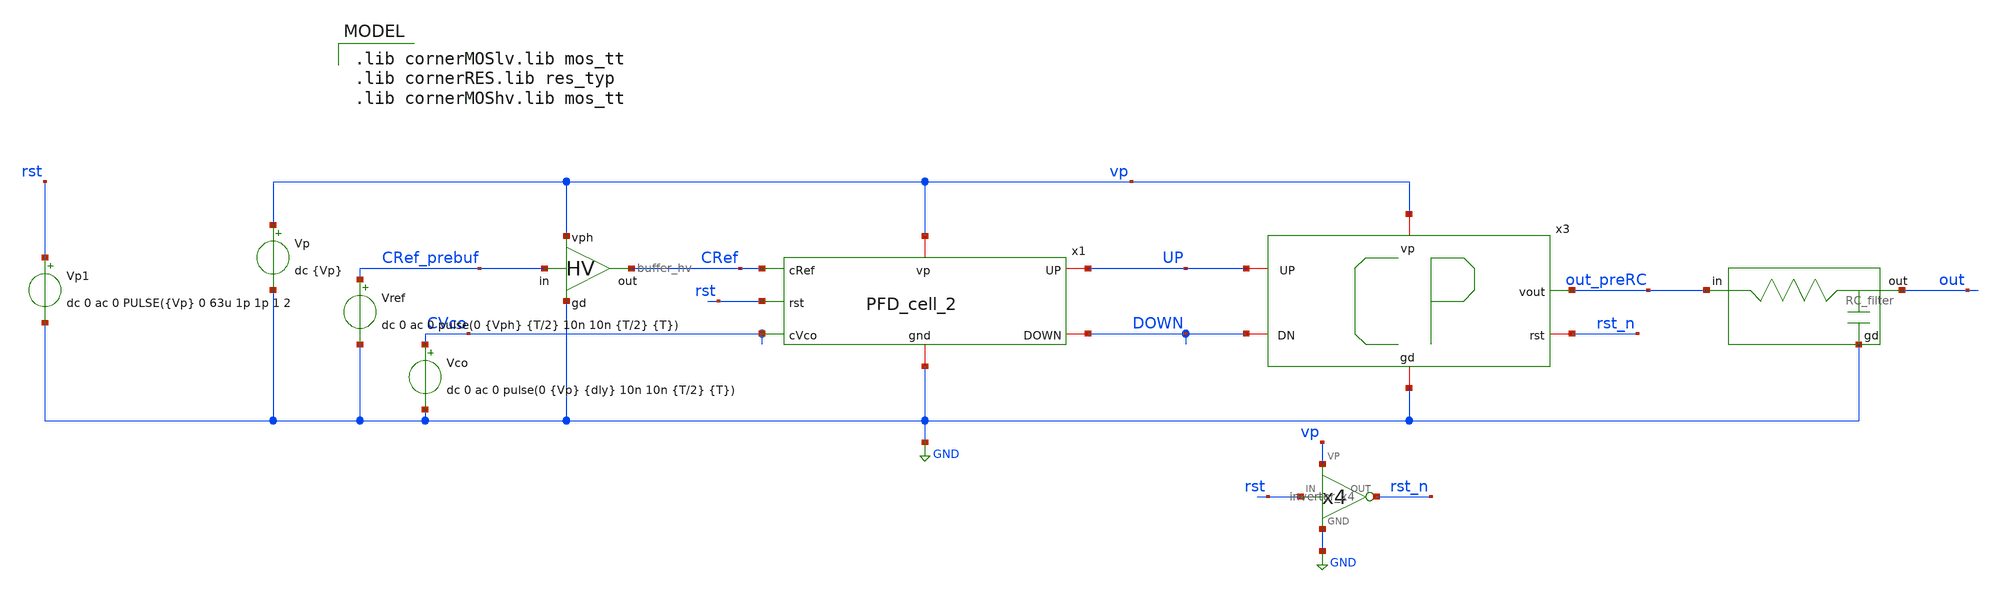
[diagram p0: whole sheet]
** sch_path: schematics/PFD/PFD_CP_tb.sch
**.subckt PFD_CP_tb
Vref CRef_prebuf GND dc 0 ac 0 pulse(0 {Vph} {T/2} 10n 10n {T/2} {T})
Vco CVco GND dc 0 ac 0 pulse(0 {Vp} {dly} 10n 10n {T/2} {T})
Vp vp GND dc {Vp}
x2 vp CRef_prebuf CRef GND buffer_hv
x1 GND vp CRef UP DOWN CVco rst PFD_cell_2
x3 vp UP out_preRC DOWN rst_n GND charge_pump_cell
Vp1 rst GND dc 0 ac 0 PULSE({Vp} 0 63u 1p 1p 1 2
x4 rst rst_n vp GND inverter_x4
x5 out out_preRC GND RC_filter
**** begin user architecture code
 .lib cornerMOSlv.lib mos_tt
.lib cornerRES.lib res_typ
.lib cornerMOShv.lib mos_tt



.temp=25
.param T = 31.25u
.param dly=1u
.param Vp=1.2
.param Vph=3.3
.control
save all
tran 25n 300u

meas tran pw_up avg v(UP) from=100u to=1m
meas tran pw_down avg v(DOWN) from=100u to=300u
plot v(pw_up) v(pw_down) v(out)
write PFD_tb.raw
.endc


**** end user architecture code
**.ends
.GLOBAL GND
.end
